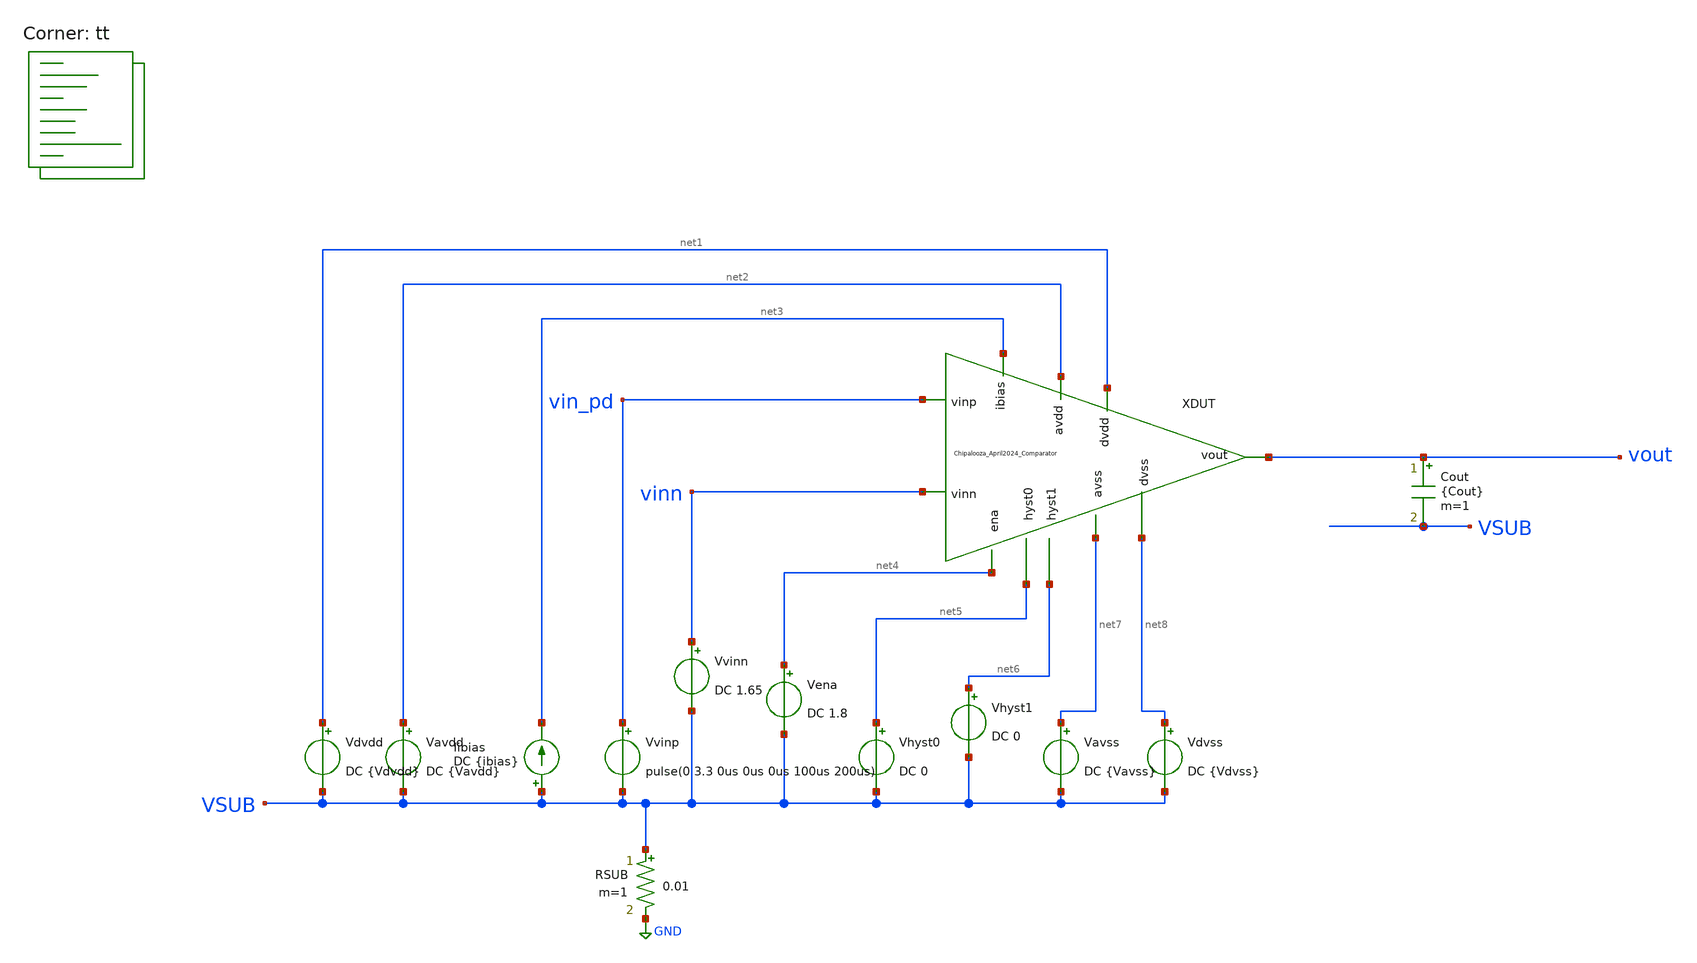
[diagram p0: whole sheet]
** sch_path: Chipalooza_April2024_Comparator/xschem/TB_propDelay.sch
**.subckt TB_propDelay
Vavdd net2 VSUB DC {Vavdd}
Cout vout VSUB {Cout} m=1
Vdvdd net1 VSUB DC {Vdvdd}
Vena net4 VSUB DC 1.8
Vhyst0 net5 VSUB DC 0
Vhyst1 net6 VSUB DC 0
Vavss net7 VSUB DC {Vavss}
Vdvss net8 VSUB DC {Vdvss}
RSUB VSUB GND 0.01 m=1
Iibias VSUB net3 DC {ibias}
XDUT net5 net6 net2 vin_pd net7 vinn net1 net8 vout net3 net4 Chipalooza_April2024_Comparator
Vvinp vin_pd VSUB pulse(0 3.3 0us 0us 0us 100us 200us)
Vvinn vinn VSUB DC 1.65
**** begin user architecture code
.lib $::SKYWATER_MODELS/sky130.lib.spice tt

* this option enables mos model bin
* selection based on W/NF instead of W
*.option wnflag=1
.option savecurrents
.option save all

.control

.param vdvdd=1.8 vavdd=3.3 cout=1f
.param ibias=1u ena=1 Vhyst_0=0 Vhyst_1=0
.param vavss=0 vdvss=0
.param Vcm=0


tran 0.1u 100u
plot v(vout) v(vin_pd)


meas tran propdelay TRIG AT=0.1u TARG v(vout) VAL=1.62 CROSS=1



write TB_propDelay.raw


*quit 0

.endc


**** end user architecture code
**.ends

* expanding   symbol:  Chipalooza_April2024_Comparator.sym # of pins=11
** sym_path: Chipalooza_April2024_Comparator/xschem/Chipalooza_April2024_Comparator.sym
** sch_path: Chipalooza_April2024_Comparator/xschem/Chipalooza_April2024_Comparator.sch
.subckt Chipalooza_April2024_Comparator hyst0 hyst1 avdd vinp avss vinn dvdd dvss vout ibias ena
*.ipin vinp
*.ipin vinn
*.ipin hyst0
*.ipin hyst1
*.ipin avdd
*.ipin avss
*.ipin dvdd
*.ipin dvss
*.opin vout
*.ipin ena
*.ipin ibias
XM29 SumOutBar SumOut dvdd dvdd sky130_fd_pr__pfet_01v8 L=1 W=2 nf=1 ad='int((nf+1)/2) * W/nf * 0.29'
+ as='int((nf+2)/2) * W/nf * 0.29' pd='2*int((nf+1)/2) * (W/nf + 0.29)' ps='2*int((nf+2)/2) * (W/nf + 0.29)'
+ nrd='0.29 / W' nrs='0.29 / W' sa=0 sb=0 sd=0 mult=2 m=2
XM30 SumOutBar SumOut avssi dvss sky130_fd_pr__nfet_01v8 L=1 W=2 nf=1 ad='int((nf+1)/2) * W/nf * 0.29'
+ as='int((nf+2)/2) * W/nf * 0.29' pd='2*int((nf+1)/2) * (W/nf + 0.29)' ps='2*int((nf+2)/2) * (W/nf + 0.29)'
+ nrd='0.29 / W' nrs='0.29 / W' sa=0 sb=0 sd=0 mult=2 m=2
XM25 net2 ibias avssi avss sky130_fd_pr__nfet_g5v0d10v5 L=1 W=1 nf=1 ad='int((nf+1)/2) * W/nf * 0.29'
+ as='int((nf+2)/2) * W/nf * 0.29' pd='2*int((nf+1)/2) * (W/nf + 0.29)' ps='2*int((nf+2)/2) * (W/nf + 0.29)'
+ nrd='0.29 / W' nrs='0.29 / W' sa=0 sb=0 sd=0 mult=2 m=2
C1 avss 0 2p m=1
XM38 avssi ena avss avss sky130_fd_pr__nfet_g5v0d10v5 L=1 W=32 nf=1 ad='int((nf+1)/2) * W/nf * 0.29'
+ as='int((nf+2)/2) * W/nf * 0.29' pd='2*int((nf+1)/2) * (W/nf + 0.29)' ps='2*int((nf+2)/2) * (W/nf + 0.29)'
+ nrd='0.29 / W' nrs='0.29 / W' sa=0 sb=0 sd=0 mult=8 m=8
XM39 net3 ibias avssi avss sky130_fd_pr__nfet_g5v0d10v5 L=1 W=3 nf=1 ad='int((nf+1)/2) * W/nf * 0.29'
+ as='int((nf+2)/2) * W/nf * 0.29' pd='2*int((nf+1)/2) * (W/nf + 0.29)' ps='2*int((nf+2)/2) * (W/nf + 0.29)'
+ nrd='0.29 / W' nrs='0.29 / W' sa=0 sb=0 sd=0 mult=2 m=2
XM16 vout SumOutBar dvdd dvdd sky130_fd_pr__pfet_01v8 L=1 W=2 nf=1 ad='int((nf+1)/2) * W/nf * 0.29' as='int((nf+2)/2) * W/nf * 0.29'
+ pd='2*int((nf+1)/2) * (W/nf + 0.29)' ps='2*int((nf+2)/2) * (W/nf + 0.29)' nrd='0.29 / W' nrs='0.29 / W'
+ sa=0 sb=0 sd=0 mult=2 m=2
XM18 vout SumOutBar avssi dvss sky130_fd_pr__nfet_01v8 L=1 W=2 nf=1 ad='int((nf+1)/2) * W/nf * 0.29'
+ as='int((nf+2)/2) * W/nf * 0.29' pd='2*int((nf+1)/2) * (W/nf + 0.29)' ps='2*int((nf+2)/2) * (W/nf + 0.29)'
+ nrd='0.29 / W' nrs='0.29 / W' sa=0 sb=0 sd=0 mult=2 m=2
XM4 SourceBias2 SourceBias2 avdd avdd sky130_fd_pr__pfet_g5v0d10v5 L=1 W=2 nf=1 ad='int((nf+1)/2) * W/nf * 0.29'
+ as='int((nf+2)/2) * W/nf * 0.29' pd='2*int((nf+1)/2) * (W/nf + 0.29)' ps='2*int((nf+2)/2) * (W/nf + 0.29)'
+ nrd='0.29 / W' nrs='0.29 / W' sa=0 sb=0 sd=0 mult=2 m=2
XM5 N1 SourceBias2 avdd avdd sky130_fd_pr__pfet_g5v0d10v5 L=1 W=2 nf=1 ad='int((nf+1)/2) * W/nf * 0.29'
+ as='int((nf+2)/2) * W/nf * 0.29' pd='2*int((nf+1)/2) * (W/nf + 0.29)' ps='2*int((nf+2)/2) * (W/nf + 0.29)'
+ nrd='0.29 / W' nrs='0.29 / W' sa=0 sb=0 sd=0 mult=2 m=2
XM6 N2 SourceBias2 avdd avdd sky130_fd_pr__pfet_g5v0d10v5 L=1 W=2 nf=1 ad='int((nf+1)/2) * W/nf * 0.29'
+ as='int((nf+2)/2) * W/nf * 0.29' pd='2*int((nf+1)/2) * (W/nf + 0.29)' ps='2*int((nf+2)/2) * (W/nf + 0.29)'
+ nrd='0.29 / W' nrs='0.29 / W' sa=0 sb=0 sd=0 mult=2 m=2
XM7 SumOut Bias1 N2 avdd sky130_fd_pr__pfet_g5v0d10v5 L=1 W=2 nf=1 ad='int((nf+1)/2) * W/nf * 0.29' as='int((nf+2)/2) * W/nf * 0.29'
+ pd='2*int((nf+1)/2) * (W/nf + 0.29)' ps='2*int((nf+2)/2) * (W/nf + 0.29)' nrd='0.29 / W' nrs='0.29 / W'
+ sa=0 sb=0 sd=0 mult=2 m=2
XM8 Sum Bias1 N1 avdd sky130_fd_pr__pfet_g5v0d10v5 L=1 W=2 nf=1 ad='int((nf+1)/2) * W/nf * 0.29' as='int((nf+2)/2) * W/nf * 0.29'
+ pd='2*int((nf+1)/2) * (W/nf + 0.29)' ps='2*int((nf+2)/2) * (W/nf + 0.29)' nrd='0.29 / W' nrs='0.29 / W'
+ sa=0 sb=0 sd=0 mult=2 m=2
XM9 SumOut Bias2 P2 avss sky130_fd_pr__nfet_g5v0d10v5 L=1 W=2 nf=1 ad='int((nf+1)/2) * W/nf * 0.29' as='int((nf+2)/2) * W/nf * 0.29'
+ pd='2*int((nf+1)/2) * (W/nf + 0.29)' ps='2*int((nf+2)/2) * (W/nf + 0.29)' nrd='0.29 / W' nrs='0.29 / W'
+ sa=0 sb=0 sd=0 mult=2 m=2
XM10 Sum Bias2 P1 avss sky130_fd_pr__nfet_g5v0d10v5 L=1 W=2 nf=1 ad='int((nf+1)/2) * W/nf * 0.29' as='int((nf+2)/2) * W/nf * 0.29'
+ pd='2*int((nf+1)/2) * (W/nf + 0.29)' ps='2*int((nf+2)/2) * (W/nf + 0.29)' nrd='0.29 / W' nrs='0.29 / W'
+ sa=0 sb=0 sd=0 mult=2 m=2
XM11 P2 Sum avssi avss sky130_fd_pr__nfet_g5v0d10v5 L=1 W=2 nf=1 ad='int((nf+1)/2) * W/nf * 0.29' as='int((nf+2)/2) * W/nf * 0.29'
+ pd='2*int((nf+1)/2) * (W/nf + 0.29)' ps='2*int((nf+2)/2) * (W/nf + 0.29)' nrd='0.29 / W' nrs='0.29 / W'
+ sa=0 sb=0 sd=0 mult=2 m=2
XM12 P1 Sum avssi avss sky130_fd_pr__nfet_g5v0d10v5 L=1 W=2 nf=1 ad='int((nf+1)/2) * W/nf * 0.29' as='int((nf+2)/2) * W/nf * 0.29'
+ pd='2*int((nf+1)/2) * (W/nf + 0.29)' ps='2*int((nf+2)/2) * (W/nf + 0.29)' nrd='0.29 / W' nrs='0.29 / W'
+ sa=0 sb=0 sd=0 mult=2 m=2
XM2 P2 vinn psource_input avdd sky130_fd_pr__pfet_g5v0d10v5 L=1 W=4 nf=1 ad='int((nf+1)/2) * W/nf * 0.29'
+ as='int((nf+2)/2) * W/nf * 0.29' pd='2*int((nf+1)/2) * (W/nf + 0.29)' ps='2*int((nf+2)/2) * (W/nf + 0.29)'
+ nrd='0.29 / W' nrs='0.29 / W' sa=0 sb=0 sd=0 mult=2 m=2
XM3 P1 vinp psource_input avdd sky130_fd_pr__pfet_g5v0d10v5 L=1 W=4 nf=1 ad='int((nf+1)/2) * W/nf * 0.29'
+ as='int((nf+2)/2) * W/nf * 0.29' pd='2*int((nf+1)/2) * (W/nf + 0.29)' ps='2*int((nf+2)/2) * (W/nf + 0.29)'
+ nrd='0.29 / W' nrs='0.29 / W' sa=0 sb=0 sd=0 mult=2 m=2
XM14 psource_input net4 avdd avdd sky130_fd_pr__pfet_g5v0d10v5 L=1 W=12 nf=1 ad='int((nf+1)/2) * W/nf * 0.29'
+ as='int((nf+2)/2) * W/nf * 0.29' pd='2*int((nf+1)/2) * (W/nf + 0.29)' ps='2*int((nf+2)/2) * (W/nf + 0.29)'
+ nrd='0.29 / W' nrs='0.29 / W' sa=0 sb=0 sd=0 mult=4 m=4
XM15 net4 net4 avdd avdd sky130_fd_pr__pfet_g5v0d10v5 L=1 W=8 nf=1 ad='int((nf+1)/2) * W/nf * 0.29' as='int((nf+2)/2) * W/nf * 0.29'
+ pd='2*int((nf+1)/2) * (W/nf + 0.29)' ps='2*int((nf+2)/2) * (W/nf + 0.29)' nrd='0.29 / W' nrs='0.29 / W'
+ sa=0 sb=0 sd=0 mult=2 m=2
XM17 nbias_tail PBias psource_input avdd sky130_fd_pr__pfet_g5v0d10v5 L=1 W=8 nf=1 ad='int((nf+1)/2) * W/nf * 0.29'
+ as='int((nf+2)/2) * W/nf * 0.29' pd='2*int((nf+1)/2) * (W/nf + 0.29)' ps='2*int((nf+2)/2) * (W/nf + 0.29)'
+ nrd='0.29 / W' nrs='0.29 / W' sa=0 sb=0 sd=0 mult=2 m=2
XM20 N1 vinp SourceBias0 avss sky130_fd_pr__nfet_g5v0d10v5 L=4 W=16 nf=1 ad='int((nf+1)/2) * W/nf * 0.29'
+ as='int((nf+2)/2) * W/nf * 0.29' pd='2*int((nf+1)/2) * (W/nf + 0.29)' ps='2*int((nf+2)/2) * (W/nf + 0.29)'
+ nrd='0.29 / W' nrs='0.29 / W' sa=0 sb=0 sd=0 mult=2 m=2
XM21 N2 vinn SourceBias0 avss sky130_fd_pr__nfet_g5v0d10v5 L=4 W=16 nf=1 ad='int((nf+1)/2) * W/nf * 0.29'
+ as='int((nf+2)/2) * W/nf * 0.29' pd='2*int((nf+1)/2) * (W/nf + 0.29)' ps='2*int((nf+2)/2) * (W/nf + 0.29)'
+ nrd='0.29 / W' nrs='0.29 / W' sa=0 sb=0 sd=0 mult=2 m=2
XM22 SourceBias0 nbias_tail avssi avss sky130_fd_pr__nfet_g5v0d10v5 L=1 W=12 nf=1 ad='int((nf+1)/2) * W/nf * 0.29'
+ as='int((nf+2)/2) * W/nf * 0.29' pd='2*int((nf+1)/2) * (W/nf + 0.29)' ps='2*int((nf+2)/2) * (W/nf + 0.29)'
+ nrd='0.29 / W' nrs='0.29 / W' sa=0 sb=0 sd=0 mult=4 m=4
XM23 nbias_tail nbias_tail avssi avss sky130_fd_pr__nfet_g5v0d10v5 L=1 W=12 nf=1 ad='int((nf+1)/2) * W/nf * 0.29'
+ as='int((nf+2)/2) * W/nf * 0.29' pd='2*int((nf+1)/2) * (W/nf + 0.29)' ps='2*int((nf+2)/2) * (W/nf + 0.29)'
+ nrd='0.29 / W' nrs='0.29 / W' sa=0 sb=0 sd=0 mult=2 m=2
XM28 net4 hyst_bias0 SourceBias0 avss sky130_fd_pr__nfet_g5v0d10v5 L=1 W=4 nf=1 ad='int((nf+1)/2) * W/nf * 0.29'
+ as='int((nf+2)/2) * W/nf * 0.29' pd='2*int((nf+1)/2) * (W/nf + 0.29)' ps='2*int((nf+2)/2) * (W/nf + 0.29)'
+ nrd='0.29 / W' nrs='0.29 / W' sa=0 sb=0 sd=0 mult=2 m=2
XM45 SourceBias1 ibias avssi avss sky130_fd_pr__nfet_g5v0d10v5 L=1 W=3 nf=1 ad='int((nf+1)/2) * W/nf * 0.29'
+ as='int((nf+2)/2) * W/nf * 0.29' pd='2*int((nf+1)/2) * (W/nf + 0.29)' ps='2*int((nf+2)/2) * (W/nf + 0.29)'
+ nrd='0.29 / W' nrs='0.29 / W' sa=0 sb=0 sd=0 mult=2 m=2
XM46 SourceBias1 SourceBias1 avdd avdd sky130_fd_pr__pfet_g5v0d10v5 L=1 W=12 nf=1 ad='int((nf+1)/2) * W/nf * 0.29'
+ as='int((nf+2)/2) * W/nf * 0.29' pd='2*int((nf+1)/2) * (W/nf + 0.29)' ps='2*int((nf+2)/2) * (W/nf + 0.29)'
+ nrd='0.29 / W' nrs='0.29 / W' sa=0 sb=0 sd=0 mult=4 m=4
XM47 psource_input SourceBias1 avdd avdd sky130_fd_pr__pfet_g5v0d10v5 L=1 W=12 nf=1 ad='int((nf+1)/2) * W/nf * 0.29'
+ as='int((nf+2)/2) * W/nf * 0.29' pd='2*int((nf+1)/2) * (W/nf + 0.29)' ps='2*int((nf+2)/2) * (W/nf + 0.29)'
+ nrd='0.29 / W' nrs='0.29 / W' sa=0 sb=0 sd=0 mult=4 m=4
XM48 SourceBias2 ibias avssi avss sky130_fd_pr__nfet_g5v0d10v5 L=1 W=6 nf=1 ad='int((nf+1)/2) * W/nf * 0.29'
+ as='int((nf+2)/2) * W/nf * 0.29' pd='2*int((nf+1)/2) * (W/nf + 0.29)' ps='2*int((nf+2)/2) * (W/nf + 0.29)'
+ nrd='0.29 / W' nrs='0.29 / W' sa=0 sb=0 sd=0 mult=2 m=2
XM63 PBias PBias avdd avdd sky130_fd_pr__pfet_g5v0d10v5 L=5 W=3 nf=1 ad='int((nf+1)/2) * W/nf * 0.29'
+ as='int((nf+2)/2) * W/nf * 0.29' pd='2*int((nf+1)/2) * (W/nf + 0.29)' ps='2*int((nf+2)/2) * (W/nf + 0.29)'
+ nrd='0.29 / W' nrs='0.29 / W' sa=0 sb=0 sd=0 mult=1 m=1
XM62 avdd Bias4 SourceBias3 avss sky130_fd_pr__nfet_g5v0d10v5 L=1 W=4 nf=1 ad='int((nf+1)/2) * W/nf * 0.29'
+ as='int((nf+2)/2) * W/nf * 0.29' pd='2*int((nf+1)/2) * (W/nf + 0.29)' ps='2*int((nf+2)/2) * (W/nf + 0.29)'
+ nrd='0.29 / W' nrs='0.29 / W' sa=0 sb=0 sd=0 mult=2 m=2
XM64 PBias Bias4 SourceBias3 avss sky130_fd_pr__nfet_g5v0d10v5 L=1 W=4 nf=1 ad='int((nf+1)/2) * W/nf * 0.29'
+ as='int((nf+2)/2) * W/nf * 0.29' pd='2*int((nf+1)/2) * (W/nf + 0.29)' ps='2*int((nf+2)/2) * (W/nf + 0.29)'
+ nrd='0.29 / W' nrs='0.29 / W' sa=0 sb=0 sd=0 mult=2 m=2
XM65 SourceBias3 ibias avssi avss sky130_fd_pr__nfet_g5v0d10v5 L=1 W=1 nf=1 ad='int((nf+1)/2) * W/nf * 0.29'
+ as='int((nf+2)/2) * W/nf * 0.29' pd='2*int((nf+1)/2) * (W/nf + 0.29)' ps='2*int((nf+2)/2) * (W/nf + 0.29)'
+ nrd='0.29 / W' nrs='0.29 / W' sa=0 sb=0 sd=0 mult=2 m=2
XM76 Bias1 ibias avssi avss sky130_fd_pr__nfet_g5v0d10v5 L=1 W=3 nf=1 ad='int((nf+1)/2) * W/nf * 0.29'
+ as='int((nf+2)/2) * W/nf * 0.29' pd='2*int((nf+1)/2) * (W/nf + 0.29)' ps='2*int((nf+2)/2) * (W/nf + 0.29)'
+ nrd='0.29 / W' nrs='0.29 / W' sa=0 sb=0 sd=0 mult=2 m=2
XM77 SourceBias5 ibias avssi avss sky130_fd_pr__nfet_g5v0d10v5 L=1 W=3 nf=1 ad='int((nf+1)/2) * W/nf * 0.29'
+ as='int((nf+2)/2) * W/nf * 0.29' pd='2*int((nf+1)/2) * (W/nf + 0.29)' ps='2*int((nf+2)/2) * (W/nf + 0.29)'
+ nrd='0.29 / W' nrs='0.29 / W' sa=0 sb=0 sd=0 mult=2 m=2
XM78 SourceBias6 ibias avssi avss sky130_fd_pr__nfet_g5v0d10v5 L=1 W=3 nf=1 ad='int((nf+1)/2) * W/nf * 0.29'
+ as='int((nf+2)/2) * W/nf * 0.29' pd='2*int((nf+1)/2) * (W/nf + 0.29)' ps='2*int((nf+2)/2) * (W/nf + 0.29)'
+ nrd='0.29 / W' nrs='0.29 / W' sa=0 sb=0 sd=0 mult=2 m=2
XM79 SourceBias7 ibias avssi avss sky130_fd_pr__nfet_g5v0d10v5 L=1 W=3 nf=1 ad='int((nf+1)/2) * W/nf * 0.29'
+ as='int((nf+2)/2) * W/nf * 0.29' pd='2*int((nf+1)/2) * (W/nf + 0.29)' ps='2*int((nf+2)/2) * (W/nf + 0.29)'
+ nrd='0.29 / W' nrs='0.29 / W' sa=0 sb=0 sd=0 mult=2 m=2
XM81 Bias5 ibias avssi avss sky130_fd_pr__nfet_g5v0d10v5 L=1 W=3 nf=1 ad='int((nf+1)/2) * W/nf * 0.29'
+ as='int((nf+2)/2) * W/nf * 0.29' pd='2*int((nf+1)/2) * (W/nf + 0.29)' ps='2*int((nf+2)/2) * (W/nf + 0.29)'
+ nrd='0.29 / W' nrs='0.29 / W' sa=0 sb=0 sd=0 mult=2 m=2
XM82 Bias4 ibias avssi avss sky130_fd_pr__nfet_g5v0d10v5 L=1 W=3 nf=1 ad='int((nf+1)/2) * W/nf * 0.29'
+ as='int((nf+2)/2) * W/nf * 0.29' pd='2*int((nf+1)/2) * (W/nf + 0.29)' ps='2*int((nf+2)/2) * (W/nf + 0.29)'
+ nrd='0.29 / W' nrs='0.29 / W' sa=0 sb=0 sd=0 mult=2 m=2
XM83 SourceBias10 ibias avssi avss sky130_fd_pr__nfet_g5v0d10v5 L=1 W=3 nf=1 ad='int((nf+1)/2) * W/nf * 0.29'
+ as='int((nf+2)/2) * W/nf * 0.29' pd='2*int((nf+1)/2) * (W/nf + 0.29)' ps='2*int((nf+2)/2) * (W/nf + 0.29)'
+ nrd='0.29 / W' nrs='0.29 / W' sa=0 sb=0 sd=0 mult=2 m=2
XM54 M55Source M55Drain avssi avss sky130_fd_pr__nfet_g5v0d10v5 L=1.5 W=6 nf=1 ad='int((nf+1)/2) * W/nf * 0.29'
+ as='int((nf+2)/2) * W/nf * 0.29' pd='2*int((nf+1)/2) * (W/nf + 0.29)' ps='2*int((nf+2)/2) * (W/nf + 0.29)'
+ nrd='0.29 / W' nrs='0.29 / W' sa=0 sb=0 sd=0 mult=2 m=2
XM55 M55Drain Bias2 M55Source avss sky130_fd_pr__nfet_g5v0d10v5 L=1 W=9 nf=1 ad='int((nf+1)/2) * W/nf * 0.29'
+ as='int((nf+2)/2) * W/nf * 0.29' pd='2*int((nf+1)/2) * (W/nf + 0.29)' ps='2*int((nf+2)/2) * (W/nf + 0.29)'
+ nrd='0.29 / W' nrs='0.29 / W' sa=0 sb=0 sd=0 mult=2 m=2
XM56 Bias2 Bias2 avssi avss sky130_fd_pr__nfet_g5v0d10v5 L=2 W=0.5 nf=1 ad='int((nf+1)/2) * W/nf * 0.29'
+ as='int((nf+2)/2) * W/nf * 0.29' pd='2*int((nf+1)/2) * (W/nf + 0.29)' ps='2*int((nf+2)/2) * (W/nf + 0.29)'
+ nrd='0.29 / W' nrs='0.29 / W' sa=0 sb=0 sd=0 mult=1 m=1
XM51 net5 net6 avdd avdd sky130_fd_pr__pfet_g5v0d10v5 L=2 W=20 nf=1 ad='int((nf+1)/2) * W/nf * 0.29'
+ as='int((nf+2)/2) * W/nf * 0.29' pd='2*int((nf+1)/2) * (W/nf + 0.29)' ps='2*int((nf+2)/2) * (W/nf + 0.29)'
+ nrd='0.29 / W' nrs='0.29 / W' sa=0 sb=0 sd=0 mult=2 m=2
XM49 net6 net6 avdd avdd sky130_fd_pr__pfet_g5v0d10v5 L=2 W=10 nf=1 ad='int((nf+1)/2) * W/nf * 0.29'
+ as='int((nf+2)/2) * W/nf * 0.29' pd='2*int((nf+1)/2) * (W/nf + 0.29)' ps='2*int((nf+2)/2) * (W/nf + 0.29)'
+ nrd='0.29 / W' nrs='0.29 / W' sa=0 sb=0 sd=0 mult=2 m=2
XM50 SourceBias4 SourceBias4 net6 avdd sky130_fd_pr__pfet_g5v0d10v5 L=1 W=10 nf=1 ad='int((nf+1)/2) * W/nf * 0.29'
+ as='int((nf+2)/2) * W/nf * 0.29' pd='2*int((nf+1)/2) * (W/nf + 0.29)' ps='2*int((nf+2)/2) * (W/nf + 0.29)'
+ nrd='0.29 / W' nrs='0.29 / W' sa=0 sb=0 sd=0 mult=2 m=2
XM52 avssi SourceBias4 net5 avdd sky130_fd_pr__pfet_g5v0d10v5 L=1 W=1 nf=1 ad='int((nf+1)/2) * W/nf * 0.29'
+ as='int((nf+2)/2) * W/nf * 0.29' pd='2*int((nf+1)/2) * (W/nf + 0.29)' ps='2*int((nf+2)/2) * (W/nf + 0.29)'
+ nrd='0.29 / W' nrs='0.29 / W' sa=0 sb=0 sd=0 mult=2 m=2
XM53 Bias1 Bias1 net5 avdd sky130_fd_pr__pfet_g5v0d10v5 L=1 W=10 nf=1 ad='int((nf+1)/2) * W/nf * 0.29'
+ as='int((nf+2)/2) * W/nf * 0.29' pd='2*int((nf+1)/2) * (W/nf + 0.29)' ps='2*int((nf+2)/2) * (W/nf + 0.29)'
+ nrd='0.29 / W' nrs='0.29 / W' sa=0 sb=0 sd=0 mult=2 m=2
XM57 net7 net8 avdd avdd sky130_fd_pr__pfet_g5v0d10v5 L=2 W=20 nf=1 ad='int((nf+1)/2) * W/nf * 0.29'
+ as='int((nf+2)/2) * W/nf * 0.29' pd='2*int((nf+1)/2) * (W/nf + 0.29)' ps='2*int((nf+2)/2) * (W/nf + 0.29)'
+ nrd='0.29 / W' nrs='0.29 / W' sa=0 sb=0 sd=0 mult=2 m=2
XM58 net8 net8 avdd avdd sky130_fd_pr__pfet_g5v0d10v5 L=2 W=10 nf=1 ad='int((nf+1)/2) * W/nf * 0.29'
+ as='int((nf+2)/2) * W/nf * 0.29' pd='2*int((nf+1)/2) * (W/nf + 0.29)' ps='2*int((nf+2)/2) * (W/nf + 0.29)'
+ nrd='0.29 / W' nrs='0.29 / W' sa=0 sb=0 sd=0 mult=2 m=2
XM59 SourceBias10 SourceBias10 net8 avdd sky130_fd_pr__pfet_g5v0d10v5 L=1 W=10 nf=1 ad='int((nf+1)/2) * W/nf * 0.29'
+ as='int((nf+2)/2) * W/nf * 0.29' pd='2*int((nf+1)/2) * (W/nf + 0.29)' ps='2*int((nf+2)/2) * (W/nf + 0.29)'
+ nrd='0.29 / W' nrs='0.29 / W' sa=0 sb=0 sd=0 mult=2 m=2
XM60 avssi SourceBias10 net7 avdd sky130_fd_pr__pfet_g5v0d10v5 L=1 W=1 nf=1 ad='int((nf+1)/2) * W/nf * 0.29'
+ as='int((nf+2)/2) * W/nf * 0.29' pd='2*int((nf+1)/2) * (W/nf + 0.29)' ps='2*int((nf+2)/2) * (W/nf + 0.29)'
+ nrd='0.29 / W' nrs='0.29 / W' sa=0 sb=0 sd=0 mult=2 m=2
XM61 Bias4 Bias4 net7 avdd sky130_fd_pr__pfet_g5v0d10v5 L=1 W=5 nf=1 ad='int((nf+1)/2) * W/nf * 0.29'
+ as='int((nf+2)/2) * W/nf * 0.29' pd='2*int((nf+1)/2) * (W/nf + 0.29)' ps='2*int((nf+2)/2) * (W/nf + 0.29)'
+ nrd='0.29 / W' nrs='0.29 / W' sa=0 sb=0 sd=0 mult=2 m=2
XM66 net9 net10 avdd avdd sky130_fd_pr__pfet_g5v0d10v5 L=2 W=20 nf=1 ad='int((nf+1)/2) * W/nf * 0.29'
+ as='int((nf+2)/2) * W/nf * 0.29' pd='2*int((nf+1)/2) * (W/nf + 0.29)' ps='2*int((nf+2)/2) * (W/nf + 0.29)'
+ nrd='0.29 / W' nrs='0.29 / W' sa=0 sb=0 sd=0 mult=2 m=2
XM67 net10 net10 avdd avdd sky130_fd_pr__pfet_g5v0d10v5 L=2 W=20 nf=1 ad='int((nf+1)/2) * W/nf * 0.29'
+ as='int((nf+2)/2) * W/nf * 0.29' pd='2*int((nf+1)/2) * (W/nf + 0.29)' ps='2*int((nf+2)/2) * (W/nf + 0.29)'
+ nrd='0.29 / W' nrs='0.29 / W' sa=0 sb=0 sd=0 mult=2 m=2
XM68 SourceBias7 SourceBias7 net10 avdd sky130_fd_pr__pfet_g5v0d10v5 L=1 W=10 nf=1 ad='int((nf+1)/2) * W/nf * 0.29'
+ as='int((nf+2)/2) * W/nf * 0.29' pd='2*int((nf+1)/2) * (W/nf + 0.29)' ps='2*int((nf+2)/2) * (W/nf + 0.29)'
+ nrd='0.29 / W' nrs='0.29 / W' sa=0 sb=0 sd=0 mult=2 m=2
XM69 avssi SourceBias7 net9 avdd sky130_fd_pr__pfet_g5v0d10v5 L=1 W=1 nf=1 ad='int((nf+1)/2) * W/nf * 0.29'
+ as='int((nf+2)/2) * W/nf * 0.29' pd='2*int((nf+1)/2) * (W/nf + 0.29)' ps='2*int((nf+2)/2) * (W/nf + 0.29)'
+ nrd='0.29 / W' nrs='0.29 / W' sa=0 sb=0 sd=0 mult=2 m=2
XM70 Bias5 Bias5 net9 avdd sky130_fd_pr__pfet_g5v0d10v5 L=1 W=5 nf=1 ad='int((nf+1)/2) * W/nf * 0.29'
+ as='int((nf+2)/2) * W/nf * 0.29' pd='2*int((nf+1)/2) * (W/nf + 0.29)' ps='2*int((nf+2)/2) * (W/nf + 0.29)'
+ nrd='0.29 / W' nrs='0.29 / W' sa=0 sb=0 sd=0 mult=2 m=2
XM72 SourceBias5 SourceBias5 avdd avdd sky130_fd_pr__pfet_g5v0d10v5 L=1 W=12 nf=1 ad='int((nf+1)/2) * W/nf * 0.29'
+ as='int((nf+2)/2) * W/nf * 0.29' pd='2*int((nf+1)/2) * (W/nf + 0.29)' ps='2*int((nf+2)/2) * (W/nf + 0.29)'
+ nrd='0.29 / W' nrs='0.29 / W' sa=0 sb=0 sd=0 mult=4 m=4
XM73 M55Drain SourceBias5 avdd avdd sky130_fd_pr__pfet_g5v0d10v5 L=1 W=12 nf=1 ad='int((nf+1)/2) * W/nf * 0.29'
+ as='int((nf+2)/2) * W/nf * 0.29' pd='2*int((nf+1)/2) * (W/nf + 0.29)' ps='2*int((nf+2)/2) * (W/nf + 0.29)'
+ nrd='0.29 / W' nrs='0.29 / W' sa=0 sb=0 sd=0 mult=4 m=4
XM74 SourceBias6 SourceBias6 avdd avdd sky130_fd_pr__pfet_g5v0d10v5 L=1 W=12 nf=1 ad='int((nf+1)/2) * W/nf * 0.29'
+ as='int((nf+2)/2) * W/nf * 0.29' pd='2*int((nf+1)/2) * (W/nf + 0.29)' ps='2*int((nf+2)/2) * (W/nf + 0.29)'
+ nrd='0.29 / W' nrs='0.29 / W' sa=0 sb=0 sd=0 mult=4 m=4
XM75 Bias2 SourceBias6 avdd avdd sky130_fd_pr__pfet_g5v0d10v5 L=1 W=12 nf=1 ad='int((nf+1)/2) * W/nf * 0.29'
+ as='int((nf+2)/2) * W/nf * 0.29' pd='2*int((nf+1)/2) * (W/nf + 0.29)' ps='2*int((nf+2)/2) * (W/nf + 0.29)'
+ nrd='0.29 / W' nrs='0.29 / W' sa=0 sb=0 sd=0 mult=4 m=4
XM1 SourceBias0 ibias avssi avss sky130_fd_pr__nfet_g5v0d10v5 L=1 W=3 nf=1 ad='int((nf+1)/2) * W/nf * 0.29'
+ as='int((nf+2)/2) * W/nf * 0.29' pd='2*int((nf+1)/2) * (W/nf + 0.29)' ps='2*int((nf+2)/2) * (W/nf + 0.29)'
+ nrd='0.29 / W' nrs='0.29 / W' sa=0 sb=0 sd=0 mult=2 m=2
XM31 net1 hyst0 net2 avss sky130_fd_pr__nfet_01v8 L=1 W=1 nf=1 ad='int((1 + 1)/2) * 1 / 1 * 0.29' as='int((1 + 2)/2) * 1 / 1 * 0.29'
+ pd='2*int((1 + 1)/2) * (1 / 1 + 0.29)' ps='2*int((1 + 2)/2) * (1 / 1 + 0.29)' nrd='0.29 / 1 ' nrs='0.29 / 1 '
+ sa=0 sb=0 sd=0 mult=2 m=2
XM32 net1 hyst1 net3 avss sky130_fd_pr__nfet_01v8 L=1 W=3 nf=1 ad='int((1 + 1)/2) * 3 / 1 * 0.29' as='int((1 + 2)/2) * 3 / 1 * 0.29'
+ pd='2*int((1 + 1)/2) * (3 / 1 + 0.29)' ps='2*int((1 + 2)/2) * (3 / 1 + 0.29)' nrd='0.29 / 3 ' nrs='0.29 / 3 '
+ sa=0 sb=0 sd=0 mult=2 m=2
XM19 N1 SumOut net1 avss sky130_fd_pr__nfet_g5v0d10v5 L=1 W=2 nf=1 ad='int((nf+1)/2) * W/nf * 0.29' as='int((nf+2)/2) * W/nf * 0.29'
+ pd='2*int((nf+1)/2) * (W/nf + 0.29)' ps='2*int((nf+2)/2) * (W/nf + 0.29)' nrd='0.29 / W' nrs='0.29 / W'
+ sa=0 sb=0 sd=0 mult=2 m=2
XM24 N2 SumOutBar net1 avss sky130_fd_pr__nfet_g5v0d10v5 L=1 W=2 nf=1 ad='int((nf+1)/2) * W/nf * 0.29'
+ as='int((nf+2)/2) * W/nf * 0.29' pd='2*int((nf+1)/2) * (W/nf + 0.29)' ps='2*int((nf+2)/2) * (W/nf + 0.29)'
+ nrd='0.29 / W' nrs='0.29 / W' sa=0 sb=0 sd=0 mult=2 m=2
XM26 ibias ibias avssi avss sky130_fd_pr__nfet_g5v0d10v5 L=1 W=3 nf=1 ad='int((nf+1)/2) * W/nf * 0.29'
+ as='int((nf+2)/2) * W/nf * 0.29' pd='2*int((nf+1)/2) * (W/nf + 0.29)' ps='2*int((nf+2)/2) * (W/nf + 0.29)'
+ nrd='0.29 / W' nrs='0.29 / W' sa=0 sb=0 sd=0 mult=2 m=2
XM27 hyst_bias0 ibias avssi avss sky130_fd_pr__nfet_g5v0d10v5 L=1 W=3 nf=1 ad='int((nf+1)/2) * W/nf * 0.29'
+ as='int((nf+2)/2) * W/nf * 0.29' pd='2*int((nf+1)/2) * (W/nf + 0.29)' ps='2*int((nf+2)/2) * (W/nf + 0.29)'
+ nrd='0.29 / W' nrs='0.29 / W' sa=0 sb=0 sd=0 mult=2 m=2
XM33 hyst_bias0 hyst_bias0 avdd avdd sky130_fd_pr__pfet_g5v0d10v5 L=1 W=3 nf=1 ad='int((nf+1)/2) * W/nf * 0.29'
+ as='int((nf+2)/2) * W/nf * 0.29' pd='2*int((nf+1)/2) * (W/nf + 0.29)' ps='2*int((nf+2)/2) * (W/nf + 0.29)'
+ nrd='0.29 / W' nrs='0.29 / W' sa=0 sb=0 sd=0 mult=2 m=2
XM34 avss hyst_bias0 avdd avdd sky130_fd_pr__pfet_g5v0d10v5 L=1 W=3 nf=1 ad='int((nf+1)/2) * W/nf * 0.29'
+ as='int((nf+2)/2) * W/nf * 0.29' pd='2*int((nf+1)/2) * (W/nf + 0.29)' ps='2*int((nf+2)/2) * (W/nf + 0.29)'
+ nrd='0.29 / W' nrs='0.29 / W' sa=0 sb=0 sd=0 mult=2 m=2
.ends

.GLOBAL GND
.end
